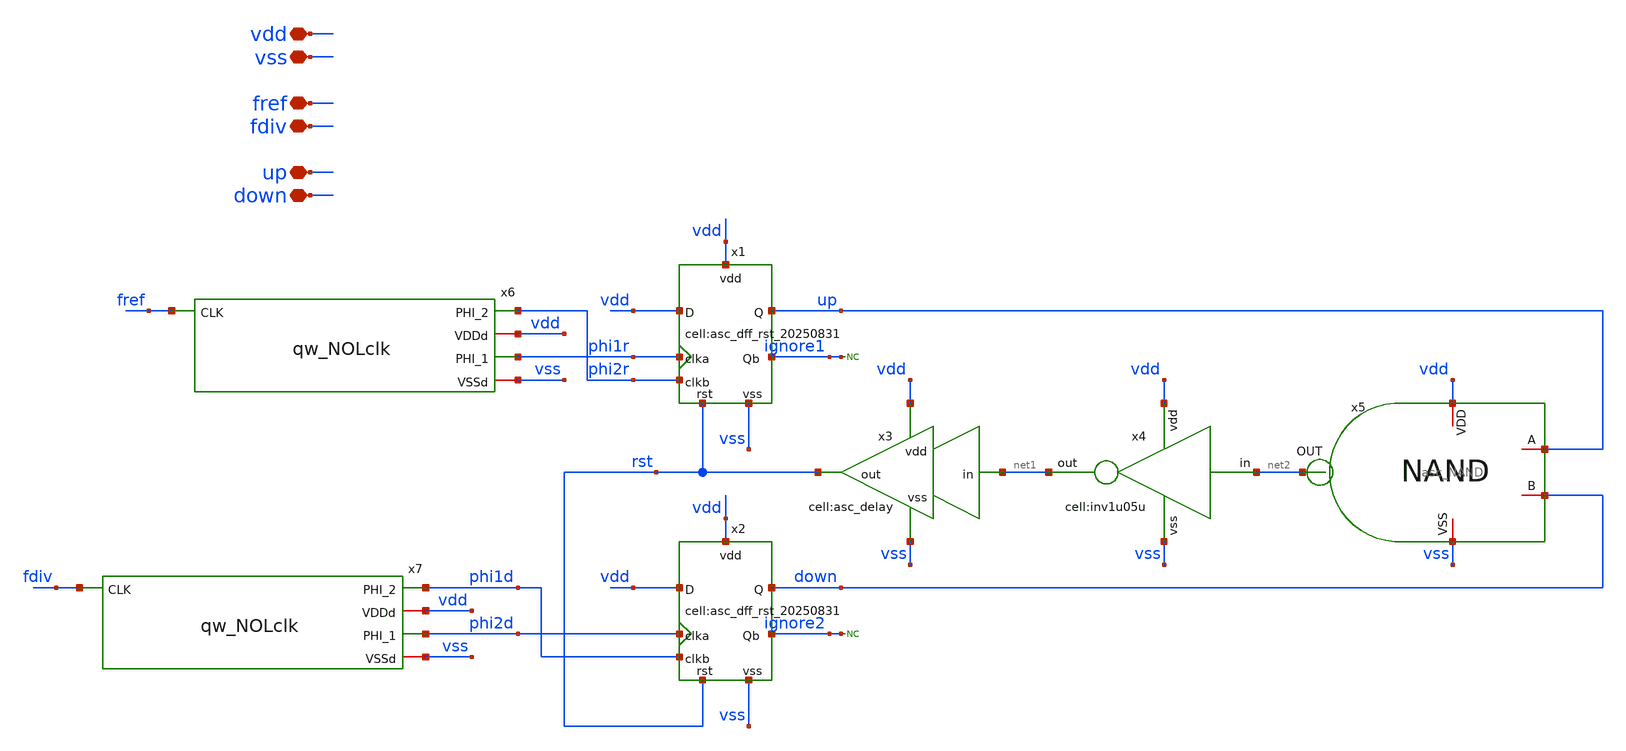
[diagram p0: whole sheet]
** sch_path: designs/libs/core_analog/asc_PFD_DFF_20250831/asc_PFD_DFF_20250831.sch
**.subckt asc_PFD_DFF_20250831 vdd vss fref fdiv up down
*.iopin vdd
*.iopin vss
*.iopin fref
*.iopin fdiv
*.iopin up
*.iopin down
x4 net2 vdd net1 vss inv1u05u
x3 net1 vss rst vdd asc_delay
x5 vdd net2 up down vss asc_NAND
* noconn ignore1
* noconn ignore2
x1 phi1r vdd ignore1 vdd vss up rst phi2r asc_dff_rst_20250831
x6 phi2r fref vdd phi1r vss qw_NOLclk
x7 phi1d fdiv vdd phi2d vss qw_NOLclk
x2 phi2d vdd ignore2 vdd vss down rst phi1d asc_dff_rst_20250831
**.ends
.end
